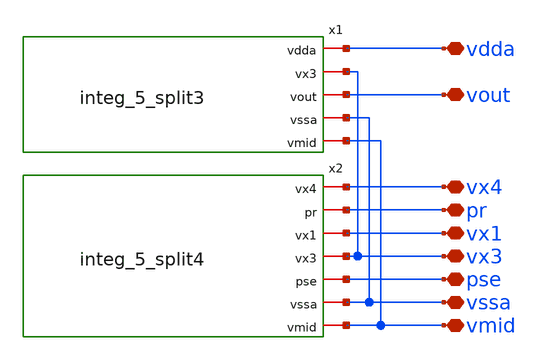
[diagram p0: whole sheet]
** sch_path: 5_Design/4_Layout/Team 5/splitUpSimulationsAndSchematics/integ_5_splitTop2.sch
**.subckt integ_5_splitTop2 vdda vout vx4 pr vx1 vx3 pse vssa vmid
*.iopin vdda
*.iopin vout
*.iopin vx4
*.iopin pr
*.iopin vx1
*.iopin vx3
*.iopin pse
*.iopin vssa
*.iopin vmid
x1 vdda vx3 vout vssa vmid integ_5_split3
x2 vx4 pr vx1 vx3 pse vssa vmid integ_5_split4
**.ends
.end
